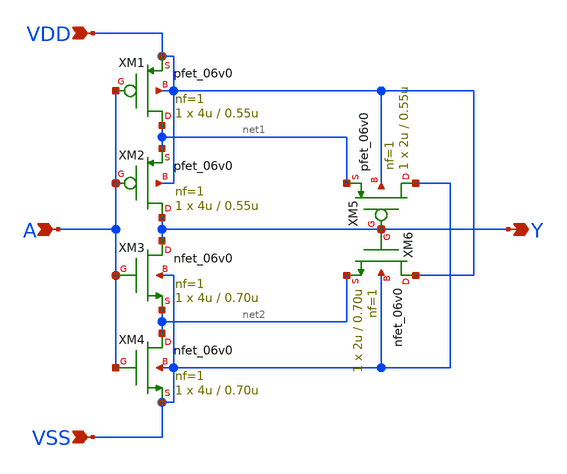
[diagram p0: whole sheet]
** sch_path: analog/xschem/schmitt.sch
**.subckt schmitt VDD VSS A Y
*.ipin VDD
*.ipin VSS
*.ipin A
*.opin Y
XM1 net1 A VDD VDD pfet_06v0 L=0.55u W=4u nf=1 ad='int((nf+1)/2) * W/nf * 0.18u' as='int((nf+2)/2) * W/nf * 0.18u'
+ pd='2*int((nf+1)/2) * (W/nf + 0.18u)' ps='2*int((nf+2)/2) * (W/nf + 0.18u)' nrd='0.18u / W' nrs='0.18u / W'
+ sa=0 sb=0 sd=0 m=1
XM2 Y A net1 VDD pfet_06v0 L=0.55u W=4u nf=1 ad='int((nf+1)/2) * W/nf * 0.18u' as='int((nf+2)/2) * W/nf * 0.18u'
+ pd='2*int((nf+1)/2) * (W/nf + 0.18u)' ps='2*int((nf+2)/2) * (W/nf + 0.18u)' nrd='0.18u / W' nrs='0.18u / W'
+ sa=0 sb=0 sd=0 m=1
XM3 Y A net2 VSS nfet_06v0 L=0.70u W=4u nf=1 ad='int((nf+1)/2) * W/nf * 0.18u' as='int((nf+2)/2) * W/nf * 0.18u'
+ pd='2*int((nf+1)/2) * (W/nf + 0.18u)' ps='2*int((nf+2)/2) * (W/nf + 0.18u)' nrd='0.18u / W' nrs='0.18u / W'
+ sa=0 sb=0 sd=0 m=1
XM4 net2 A VSS VSS nfet_06v0 L=0.70u W=4u nf=1 ad='int((nf+1)/2) * W/nf * 0.18u' as='int((nf+2)/2) * W/nf * 0.18u'
+ pd='2*int((nf+1)/2) * (W/nf + 0.18u)' ps='2*int((nf+2)/2) * (W/nf + 0.18u)' nrd='0.18u / W' nrs='0.18u / W'
+ sa=0 sb=0 sd=0 m=1
XM5 VSS Y net1 VDD pfet_06v0 L=0.55u W=2u nf=1 ad='int((nf+1)/2) * W/nf * 0.18u' as='int((nf+2)/2) * W/nf * 0.18u'
+ pd='2*int((nf+1)/2) * (W/nf + 0.18u)' ps='2*int((nf+2)/2) * (W/nf + 0.18u)' nrd='0.18u / W' nrs='0.18u / W'
+ sa=0 sb=0 sd=0 m=1
XM6 VDD Y net2 VSS nfet_06v0 L=0.70u W=2u nf=1 ad='int((nf+1)/2) * W/nf * 0.18u' as='int((nf+2)/2) * W/nf * 0.18u'
+ pd='2*int((nf+1)/2) * (W/nf + 0.18u)' ps='2*int((nf+2)/2) * (W/nf + 0.18u)' nrd='0.18u / W' nrs='0.18u / W'
+ sa=0 sb=0 sd=0 m=1
**.ends
.end
